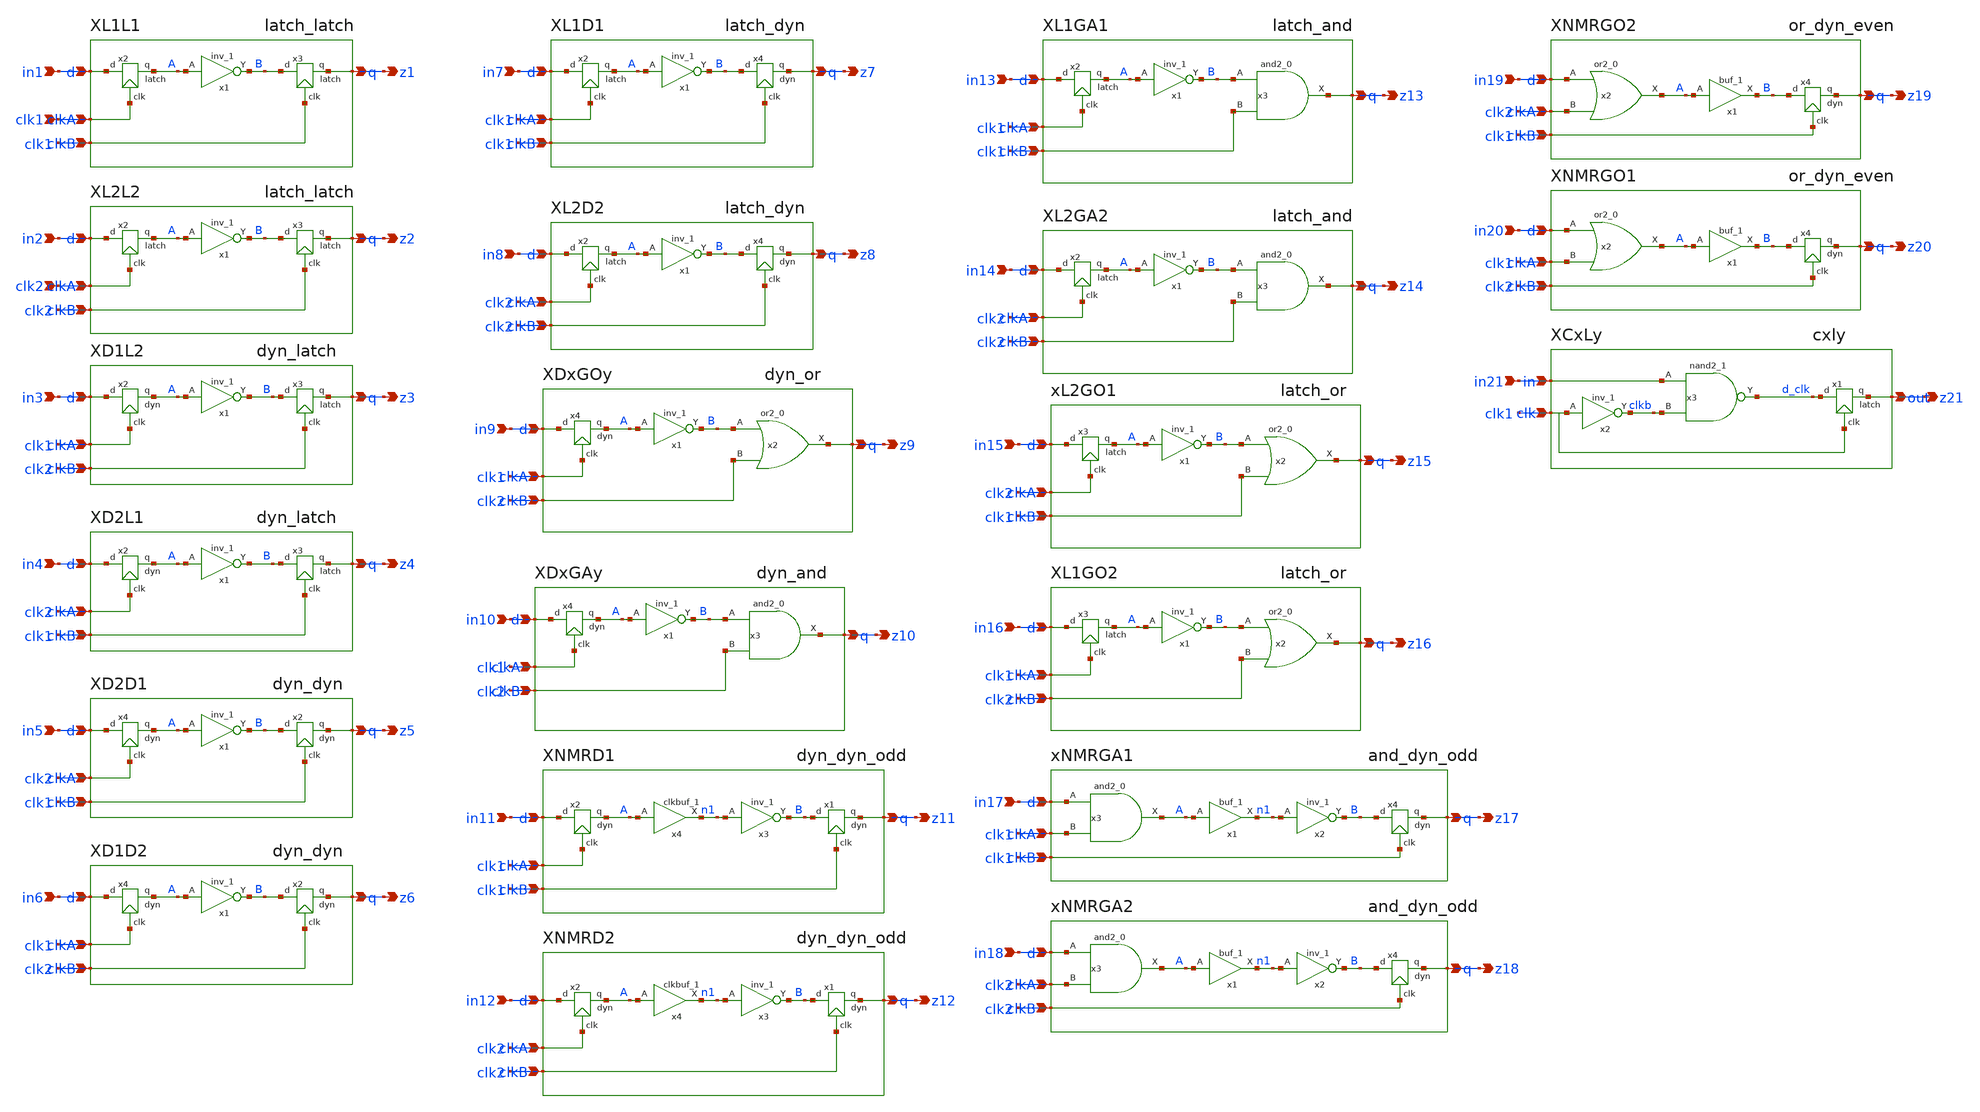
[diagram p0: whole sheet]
** sch_path: src/xe/test_cases/yxt_input_rel_test1.sch
**.subckt yxt_input_rel_test1 in1 clk1 z1 in2 z2 clk2 in3 z3 in4 z4 in5 z5 in6 z6 in7 z7 in8 z8 in9
*+ z9 in10 z10 in11 z11 in12 z12 in13 z13 in14 z14 in15 z15 in16 z16 in17 z17 in18 z18 in19 z19 in20 z20
*+ in21 z21
*.ipin in1
*.ipin clk1
*.opin z1
*.ipin in2
*.opin z2
*.ipin clk2
*.ipin in3
*.opin z3
*.ipin in4
*.opin z4
*.ipin in5
*.opin z5
*.ipin in6
*.opin z6
*.ipin in7
*.opin z7
*.ipin in8
*.opin z8
*.ipin in9
*.opin z9
*.ipin in10
*.opin z10
*.ipin in11
*.opin z11
*.ipin in12
*.opin z12
*.ipin in13
*.opin z13
*.ipin in14
*.opin z14
*.ipin in15
*.opin z15
*.ipin in16
*.opin z16
*.ipin in17
*.opin z17
*.ipin in18
*.opin z18
*.ipin in19
*.opin z19
*.ipin in20
*.opin z20
*.ipin in21
*.opin z21
XL1L1 in1 clk1 z1 clk1 latch_latch
XL2L2 in2 clk2 z2 clk2 latch_latch
XD1L2 in3 clk1 z3 clk2 dyn_latch
XD2L1 in4 clk2 z4 clk1 dyn_latch
XD2D1 in5 clk2 z5 clk1 dyn_dyn
XD1D2 in6 clk1 z6 clk2 dyn_dyn
XL1D1 in7 clk1 z7 clk1 latch_dyn
XL2D2 in8 clk2 z8 clk2 latch_dyn
XDxGOy in9 clk1 z9 clk2 dyn_or
XDxGAy in10 clk1 z10 clk2 dyn_and vcc=vcc vss=vss
XNMRD1 in11 clk1 z11 clk1 dyn_dyn_odd
XNMRD2 in12 clk2 z12 clk2 dyn_dyn_odd
XL1GA1 in13 clk1 z13 clk1 latch_and vcc=vcc vss=vss
XL2GA2 in14 clk2 z14 clk2 latch_and vcc=vcc vss=vss
xL2GO1 in15 clk2 z15 clk1 latch_or
XL1GO2 in16 clk1 z16 clk2 latch_or
xNMRGA1 in17 clk1 z17 clk1 and_dyn_odd
xNMRGA2 in18 clk2 z18 clk2 and_dyn_odd
XNMRGO2 in19 clk2 z19 clk1 or_dyn_even
XNMRGO1 in20 clk1 z20 clk2 or_dyn_even
XCxLy in21 clk1 z21 cxly vcc=vcc vss=vss
**** begin user architecture code

** opencircuitdesign pdks install

.subckt sky130_fd_sc_hd__inv_1 A VGND VNB VPB VPWR Y
X0 VGND A Y VNB sky130_fd_pr__nfet_01v8 w=650000u l=150000u
X1 VPWR A Y VPB sky130_fd_pr__pfet_01v8_hvt w=1e+06u l=150000u
.ends

.subckt sky130_fd_sc_hd__nand2_1 A B VGND VNB VPB VPWR Y
X0 Y A VPWR VPB sky130_fd_pr__pfet_01v8_hvt w=1e+06u l=150000u
X1 VPWR B Y VPB sky130_fd_pr__pfet_01v8_hvt w=1e+06u l=150000u
X2 VGND B a_113_47# VNB sky130_fd_pr__nfet_01v8 w=650000u l=150000u
X3 a_113_47# A Y VNB sky130_fd_pr__nfet_01v8 w=650000u l=150000u
.ends

.subckt sky130_fd_sc_hd__or2_0 A B VGND VNB VPB VPWR X
X0 VGND a_68_355# X VNB sky130_fd_pr__nfet_01v8 w=420000u l=150000u
X1 a_150_355# A VPWR VPB sky130_fd_pr__pfet_01v8_hvt w=420000u l=150000u
X2 VGND B a_68_355# VNB sky130_fd_pr__nfet_01v8 w=420000u l=150000u
X3 a_68_355# A VGND VNB sky130_fd_pr__nfet_01v8 w=420000u l=150000u
X4 a_68_355# B a_150_355# VPB sky130_fd_pr__pfet_01v8_hvt w=420000u l=150000u
X5 VPWR a_68_355# X VPB sky130_fd_pr__pfet_01v8_hvt w=640000u l=150000u
.ends

.subckt sky130_fd_sc_hd__buf_1 A VGND VNB VPB VPWR X
X0 VGND a_27_47# X VNB sky130_fd_pr__nfet_01v8 w=520000u l=150000u
X1 a_27_47# A VPWR VPB sky130_fd_pr__pfet_01v8_hvt w=790000u l=150000u
X2 a_27_47# A VGND VNB sky130_fd_pr__nfet_01v8 w=520000u l=150000u
X3 VPWR a_27_47# X VPB sky130_fd_pr__pfet_01v8_hvt w=790000u l=150000u
.ends

.subckt sky130_fd_sc_hd__and2_0 A B VGND VNB VPB VPWR X
X0 a_40_47# B VPWR VPB sky130_fd_pr__pfet_01v8_hvt w=420000u l=150000u
X1 a_123_47# B VGND VNB sky130_fd_pr__nfet_01v8 w=420000u l=150000u
X2 a_40_47# A a_123_47# VNB sky130_fd_pr__nfet_01v8 w=420000u l=150000u
X3 VGND a_40_47# X VNB sky130_fd_pr__nfet_01v8 w=420000u l=150000u
X4 VPWR A a_40_47# VPB sky130_fd_pr__pfet_01v8_hvt w=420000u l=150000u
X5 VPWR a_40_47# X VPB sky130_fd_pr__pfet_01v8_hvt w=640000u l=150000u
.ends

.subckt sky130_fd_sc_hd__clkbuf_1 A VGND VNB VPB VPWR X
X0 VGND A a_75_212# VNB sky130_fd_pr__nfet_01v8 w=520000u l=150000u
X1 X a_75_212# VPWR VPB sky130_fd_pr__pfet_01v8_hvt w=790000u l=150000u
X2 X a_75_212# VGND VNB sky130_fd_pr__nfet_01v8 w=520000u l=150000u
X3 VPWR A a_75_212# VPB sky130_fd_pr__pfet_01v8_hvt w=790000u l=150000u
.ends


**** end user architecture code
**.ends

* expanding   symbol:  yxt/latch_latch.sch # of pins=4
** sym_path: src/xe/test_cases/latch_latch.sch
** sch_path: src/xe/test_cases/latch_latch.sch
.subckt latch_latch d clkA q clkB
*.ipin d
*.ipin clkA
*.opin q
*.ipin clkB
x1 A vss vss vcc vcc B sky130_fd_sc_hd__inv_1
x2 clkA A d latch
x3 clkB q B latch
.ends


* expanding   symbol:  yxt/dyn_latch.sch # of pins=4
** sym_path: src/xe/test_cases/dyn_latch.sch
** sch_path: src/xe/test_cases/dyn_latch.sch
.subckt dyn_latch d clkA q clkB
*.ipin d
*.ipin clkA
*.opin q
*.ipin clkB
x1 A vss vss vcc vcc B sky130_fd_sc_hd__inv_1
x3 clkB q B latch
x2 clkA A d dyn
.ends


* expanding   symbol:  yxt/dyn_dyn.sch # of pins=4
** sym_path: src/xe/test_cases/dyn_dyn.sch
** sch_path: src/xe/test_cases/dyn_dyn.sch
.subckt dyn_dyn d clkA q clkB
*.ipin d
*.ipin clkA
*.opin q
*.ipin clkB
x1 A vss vss vcc vcc B sky130_fd_sc_hd__inv_1
x4 clkA A d dyn
x2 clkB q B dyn
.ends


* expanding   symbol:  yxt/latch_dyn.sch # of pins=4
** sym_path: src/xe/test_cases/latch_dyn.sch
** sch_path: src/xe/test_cases/latch_dyn.sch
.subckt latch_dyn d clkA q clkB
*.ipin d
*.ipin clkA
*.opin q
*.ipin clkB
x1 A vss vss vcc vcc B sky130_fd_sc_hd__inv_1
x2 clkA A d latch
x4 clkB q B dyn
.ends


* expanding   symbol:  yxt/dyn_or.sch # of pins=4
** sym_path: src/xe/test_cases/dyn_or.sch
** sch_path: src/xe/test_cases/dyn_or.sch
.subckt dyn_or d clkA q clkB
*.ipin d
*.ipin clkA
*.opin q
*.ipin clkB
x1 A vss vss vcc vcc B sky130_fd_sc_hd__inv_1
x4 clkA A d dyn
x2 B clkB vss vss vcc vcc q sky130_fd_sc_hd__or2_0
.ends


* expanding   symbol:  yxt/dyn_and.sch # of pins=4
** sym_path: src/xe/test_cases/dyn_and.sch
** sch_path: src/xe/test_cases/dyn_and.sch
.subckt dyn_and d clkA q clkB  vcc=vcc vss=vss
*.ipin d
*.ipin clkA
*.opin q
*.ipin clkB
x1 A vcc vcc vss vss B sky130_fd_sc_hd__inv_1
x3 B clkB vss vss vcc vcc q sky130_fd_sc_hd__and2_0
x4 clkA A d dyn
.ends


* expanding   symbol:  yxt/dyn_dyn_odd.sch # of pins=4
** sym_path: src/xe/test_cases/dyn_dyn_odd.sch
** sch_path: src/xe/test_cases/dyn_dyn_odd.sch
.subckt dyn_dyn_odd d clkA q clkB
*.ipin d
*.ipin clkA
*.opin q
*.ipin clkB
x2 clkA A d dyn
x4 A vss vss vcc vcc n1 sky130_fd_sc_hd__clkbuf_1
x1 clkB q B dyn
x3 n1 vss vss vcc vcc B sky130_fd_sc_hd__inv_1
.ends


* expanding   symbol:  yxt/latch_and.sch # of pins=4
** sym_path: src/xe/test_cases/latch_and.sch
** sch_path: src/xe/test_cases/latch_and.sch
.subckt latch_and d clkA q clkB  vcc=vcc vss=vss
*.ipin d
*.ipin clkA
*.opin q
*.ipin clkB
x1 A vcc vcc vss vss B sky130_fd_sc_hd__inv_1
x3 B clkB vss vss vcc vcc q sky130_fd_sc_hd__and2_0
x2 clkA A d latch
.ends


* expanding   symbol:  yxt/latch_or.sch # of pins=4
** sym_path: src/xe/test_cases/latch_or.sch
** sch_path: src/xe/test_cases/latch_or.sch
.subckt latch_or d clkA q clkB
*.ipin d
*.ipin clkA
*.opin q
*.ipin clkB
x1 A vss vss vcc vcc B sky130_fd_sc_hd__inv_1
x2 B clkB vss vss vcc vcc q sky130_fd_sc_hd__or2_0
x3 clkA A d latch
.ends


* expanding   symbol:  yxt/and_dyn_odd.sch # of pins=4
** sym_path: src/xe/test_cases/and_dyn_odd.sch
** sch_path: src/xe/test_cases/and_dyn_odd.sch
.subckt and_dyn_odd d clkA q clkB
*.ipin d
*.ipin clkA
*.opin q
*.ipin clkB
x4 clkB q B dyn
x1 A vss vss vcc vcc n1 sky130_fd_sc_hd__buf_1
x3 d clkA vss vss vcc vcc A sky130_fd_sc_hd__and2_0
x2 n1 vss vss vcc vcc B sky130_fd_sc_hd__inv_1
.ends


* expanding   symbol:  yxt/or_dyn_even.sch # of pins=4
** sym_path: src/xe/test_cases/or_dyn_even.sch
** sch_path: src/xe/test_cases/or_dyn_even.sch
.subckt or_dyn_even d clkA q clkB
*.ipin d
*.ipin clkA
*.opin q
*.ipin clkB
x2 d clkA vss vss vcc vcc A sky130_fd_sc_hd__or2_0
x4 clkB q B dyn
x1 A vss vss vcc vcc B sky130_fd_sc_hd__buf_1
.ends


* expanding   symbol:  yxt/cxly.sch # of pins=3
** sym_path: src/xe/test_cases/cxly.sch
** sch_path: src/xe/test_cases/cxly.sch
.subckt cxly in clk out  vcc=vcc vss=vss
*.ipin in
*.ipin clk
*.opin out
x2 clk VGND VNB VPB VPWR clkb sky130_fd_sc_hd__inv_1
x1 clk out d_clk latch
x3 in clkb vss vss vcc vcc d_clk sky130_fd_sc_hd__nand2_1
.ends


* expanding   symbol:  yxt/latch.sym # of pins=3
** sym_path: src/xe/test_cases/latch.sym
** sch_path: src/xe/test_cases/latch.sch
.subckt latch clk q d  vcc=vcc vss=vss
*.ipin clk
*.ipin d
*.opin q
x1 d vss vss vcc vcc db sky130_fd_sc_hd__inv_1
x2 clkb db z clk vcc vss tgate
x3 z vss vss vcc vcc q sky130_fd_sc_hd__inv_1
x6 clk vss vss vcc vcc clkb sky130_fd_sc_hd__inv_1
x4 z vss vss vcc vcc fb sky130_fd_sc_hd__inv_1
x5 fb vss vss vcc vcc z sky130_fd_sc_hd__inv_1
.ends


* expanding   symbol:  yxt/dyn.sym # of pins=3
** sym_path: src/xe/test_cases/dyn.sym
** sch_path: src/xe/test_cases/dyn.sch
.subckt dyn clk q d
*.ipin clk
*.opin q
*.ipin d
x1 z vss vss vcc vcc q sky130_fd_sc_hd__inv_1
XM1 z d net1 vss sky130_fd_pr__nfet_01v8 L=0.15 W=1 nf=1 ad='int((nf+1)/2) * W/nf * 0.29' as='int((nf+2)/2) * W/nf * 0.29'
+ pd='2*int((nf+1)/2) * (W/nf + 0.29)' ps='2*int((nf+2)/2) * (W/nf + 0.29)' nrd='0.29 / W' nrs='0.29 / W'
+ sa=0 sb=0 sd=0 mult=1 m=1
XM2 z q vcc vcc sky130_fd_pr__pfet_01v8 L=0.15 W=1 nf=1 ad='int((nf+1)/2) * W/nf * 0.29' as='int((nf+2)/2) * W/nf * 0.29'
+ pd='2*int((nf+1)/2) * (W/nf + 0.29)' ps='2*int((nf+2)/2) * (W/nf + 0.29)' nrd='0.29 / W' nrs='0.29 / W'
+ sa=0 sb=0 sd=0 mult=1 m=1
XM3 z clk vcc vcc sky130_fd_pr__pfet_01v8 L=0.15 W=1 nf=1 ad='int((nf+1)/2) * W/nf * 0.29' as='int((nf+2)/2) * W/nf * 0.29'
+ pd='2*int((nf+1)/2) * (W/nf + 0.29)' ps='2*int((nf+2)/2) * (W/nf + 0.29)' nrd='0.29 / W' nrs='0.29 / W'
+ sa=0 sb=0 sd=0 mult=1 m=1
XM4 net1 clk vss vss sky130_fd_pr__nfet_01v8 L=0.15 W=1 nf=1 ad='int((nf+1)/2) * W/nf * 0.29' as='int((nf+2)/2) * W/nf * 0.29'
+ pd='2*int((nf+1)/2) * (W/nf + 0.29)' ps='2*int((nf+2)/2) * (W/nf + 0.29)' nrd='0.29 / W' nrs='0.29 / W'
+ sa=0 sb=0 sd=0 mult=1 m=1
.ends


* expanding   symbol:  yxt/tgate.sym # of pins=4
** sym_path: src/xe/test_cases/tgate.sym
** sch_path: src/xe/test_cases/tgate.sch
.subckt tgate gp s d gn vcc vss
*.ipin s
*.ipin gp
*.ipin gn
*.opin d
XMpc d gp s vss sky130_fd_pr__pfet_01v8 L=0.15 W=1 nf=1 ad='int((nf+1)/2) * W/nf * 0.29' as='int((nf+2)/2) * W/nf * 0.29'
+ pd='2*int((nf+1)/2) * (W/nf + 0.29)' ps='2*int((nf+2)/2) * (W/nf + 0.29)' nrd='0.29 / W' nrs='0.29 / W'
+ sa=0 sb=0 sd=0 mult=7 m=7
XM15 s gn d vcc sky130_fd_pr__nfet_01v8 L=0.15 W=1 nf=1 ad='int((nf+1)/2) * W/nf * 0.29' as='int((nf+2)/2) * W/nf * 0.29'
+ pd='2*int((nf+1)/2) * (W/nf + 0.29)' ps='2*int((nf+2)/2) * (W/nf + 0.29)' nrd='0.29 / W' nrs='0.29 / W'
+ sa=0 sb=0 sd=0 mult=1 m=1
.ends

.end
